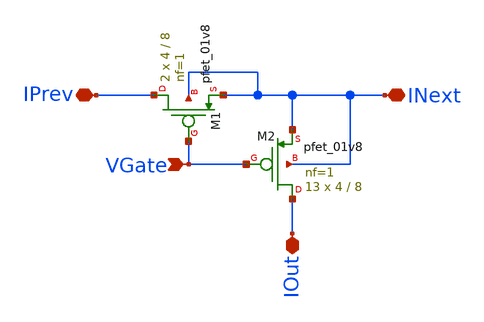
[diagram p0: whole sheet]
** sch_path: analog/xschem/BiasMultiplierCell.sch
**.subckt BiasMultiplierCell IPrev IOut INext VGate
*.iopin IPrev
*.iopin IOut
*.iopin INext
*.ipin VGate
XM1 IPrev VGate INext INext sky130_fd_pr__pfet_01v8 L=8 W=4 nf=1 ad='int((1 + 1)/2) * 4 / 1 * 0.29' as='int((1 + 2)/2) * 4 / 1 * 0.29'
+ pd='2*int((1 + 1)/2) * (4 / 1 + 0.29)' ps='2*int((1 + 2)/2) * (4 / 1 + 0.29)' nrd='0.29 / 4 ' nrs='0.29 / 4 '
+ sa=0 sb=0 sd=0 mult=2 m=2
XM2 IOut VGate INext INext sky130_fd_pr__pfet_01v8 L=8 W=4 nf=1 ad='int((1 + 1)/2) * 4 / 1 * 0.29' as='int((1 + 2)/2) * 4 / 1 * 0.29'
+ pd='2*int((1 + 1)/2) * (4 / 1 + 0.29)' ps='2*int((1 + 2)/2) * (4 / 1 + 0.29)' nrd='0.29 / 4 ' nrs='0.29 / 4 '
+ sa=0 sb=0 sd=0 mult=13 m=13
**.ends
.end
